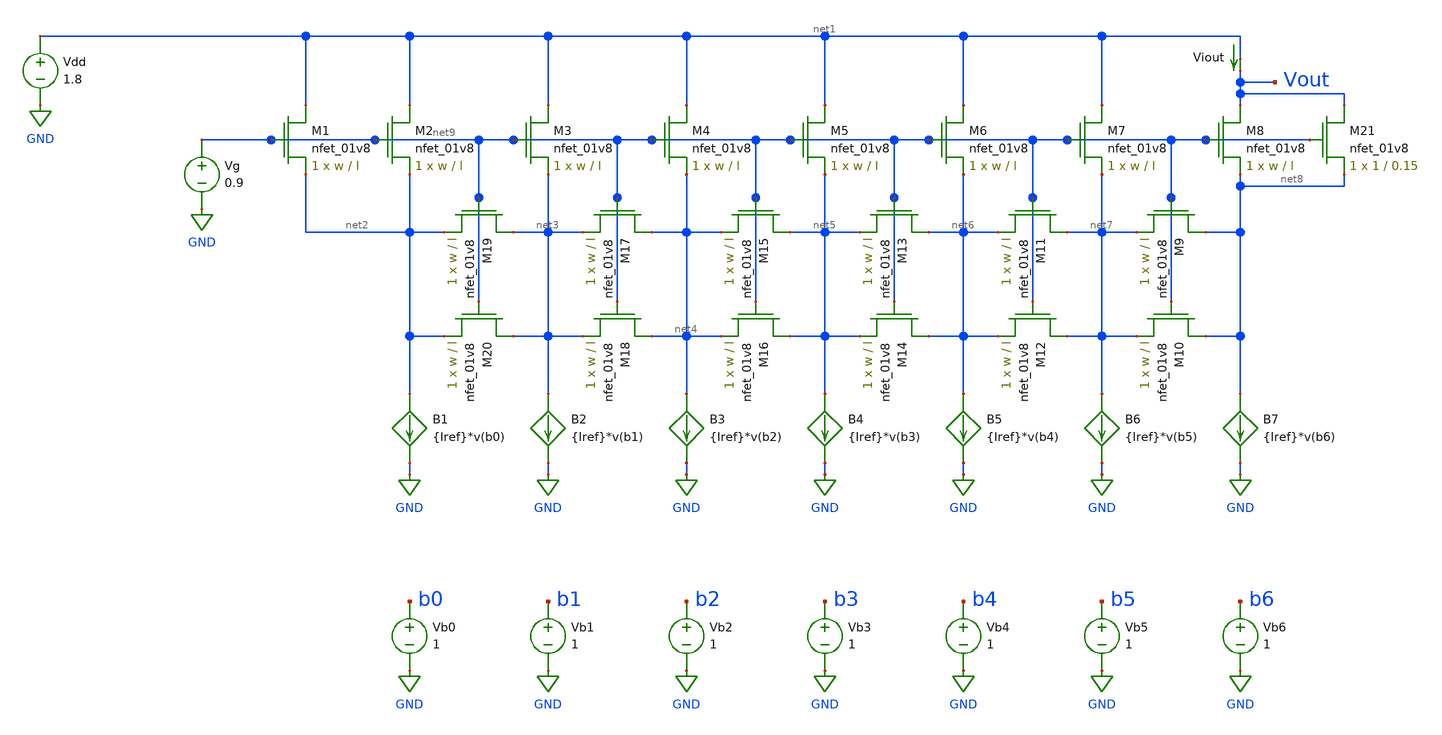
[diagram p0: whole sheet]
** sch_path: simulations/dactut/dactut/dactut_mosfet.sch
**.subckt dactut_mosfet
B1 net2 GND I={Iref}*v(b0)
Vb0 b0 GND 1
Viout net1 Vout 0
.save i(viout)
B2 net3 GND I={Iref}*v(b1)
Vb1 b1 GND 1
B3 net4 GND I={Iref}*v(b2)
Vb2 b2 GND 1
B4 net5 GND I={Iref}*v(b3)
Vb3 b3 GND 1
B5 net6 GND I={Iref}*v(b4)
Vb4 b4 GND 1
B6 net7 GND I={Iref}*v(b5)
Vb5 b5 GND 1
B7 net8 GND I={Iref}*v(b6)
Vb6 b6 GND 1
Vdd net1 GND 1.8
Vg net9 GND 0.9
XM1 net1 net9 net2 GND sky130_fd_pr__nfet_01v8 L=l W=w nf=1 ad='int((nf+1)/2) * W/nf * 0.29' as='int((nf+2)/2) * W/nf * 0.29'
+ pd='2*int((nf+1)/2) * (W/nf + 0.29)' ps='2*int((nf+2)/2) * (W/nf + 0.29)' nrd='0.29 / W' nrs='0.29 / W'
+ sa=0 sb=0 sd=0 mult=1 m=1
XM21 Vout net9 net8 GND sky130_fd_pr__nfet_01v8 L=0.15 W=1 nf=1 ad='int((nf+1)/2) * W/nf * 0.29' as='int((nf+2)/2) * W/nf * 0.29'
+ pd='2*int((nf+1)/2) * (W/nf + 0.29)' ps='2*int((nf+2)/2) * (W/nf + 0.29)' nrd='0.29 / W' nrs='0.29 / W'
+ sa=0 sb=0 sd=0 mult=1 m=1
XM2 net1 net9 net2 GND sky130_fd_pr__nfet_01v8 L=l W=w nf=1 ad='int((nf+1)/2) * W/nf * 0.29' as='int((nf+2)/2) * W/nf * 0.29'
+ pd='2*int((nf+1)/2) * (W/nf + 0.29)' ps='2*int((nf+2)/2) * (W/nf + 0.29)' nrd='0.29 / W' nrs='0.29 / W'
+ sa=0 sb=0 sd=0 mult=1 m=1
XM3 net1 net9 net3 GND sky130_fd_pr__nfet_01v8 L=l W=w nf=1 ad='int((nf+1)/2) * W/nf * 0.29' as='int((nf+2)/2) * W/nf * 0.29'
+ pd='2*int((nf+1)/2) * (W/nf + 0.29)' ps='2*int((nf+2)/2) * (W/nf + 0.29)' nrd='0.29 / W' nrs='0.29 / W'
+ sa=0 sb=0 sd=0 mult=1 m=1
XM4 net1 net9 net4 GND sky130_fd_pr__nfet_01v8 L=l W=w nf=1 ad='int((nf+1)/2) * W/nf * 0.29' as='int((nf+2)/2) * W/nf * 0.29'
+ pd='2*int((nf+1)/2) * (W/nf + 0.29)' ps='2*int((nf+2)/2) * (W/nf + 0.29)' nrd='0.29 / W' nrs='0.29 / W'
+ sa=0 sb=0 sd=0 mult=1 m=1
XM5 net1 net9 net5 GND sky130_fd_pr__nfet_01v8 L=l W=w nf=1 ad='int((nf+1)/2) * W/nf * 0.29' as='int((nf+2)/2) * W/nf * 0.29'
+ pd='2*int((nf+1)/2) * (W/nf + 0.29)' ps='2*int((nf+2)/2) * (W/nf + 0.29)' nrd='0.29 / W' nrs='0.29 / W'
+ sa=0 sb=0 sd=0 mult=1 m=1
XM6 net1 net9 net6 GND sky130_fd_pr__nfet_01v8 L=l W=w nf=1 ad='int((nf+1)/2) * W/nf * 0.29' as='int((nf+2)/2) * W/nf * 0.29'
+ pd='2*int((nf+1)/2) * (W/nf + 0.29)' ps='2*int((nf+2)/2) * (W/nf + 0.29)' nrd='0.29 / W' nrs='0.29 / W'
+ sa=0 sb=0 sd=0 mult=1 m=1
XM7 net1 net9 net7 GND sky130_fd_pr__nfet_01v8 L=l W=w nf=1 ad='int((nf+1)/2) * W/nf * 0.29' as='int((nf+2)/2) * W/nf * 0.29'
+ pd='2*int((nf+1)/2) * (W/nf + 0.29)' ps='2*int((nf+2)/2) * (W/nf + 0.29)' nrd='0.29 / W' nrs='0.29 / W'
+ sa=0 sb=0 sd=0 mult=1 m=1
XM8 Vout net9 net8 GND sky130_fd_pr__nfet_01v8 L=l W=w nf=1 ad='int((nf+1)/2) * W/nf * 0.29' as='int((nf+2)/2) * W/nf * 0.29'
+ pd='2*int((nf+1)/2) * (W/nf + 0.29)' ps='2*int((nf+2)/2) * (W/nf + 0.29)' nrd='0.29 / W' nrs='0.29 / W'
+ sa=0 sb=0 sd=0 mult=1 m=1
XM9 net8 net9 net7 GND sky130_fd_pr__nfet_01v8 L=l W=w nf=1 ad='int((nf+1)/2) * W/nf * 0.29' as='int((nf+2)/2) * W/nf * 0.29'
+ pd='2*int((nf+1)/2) * (W/nf + 0.29)' ps='2*int((nf+2)/2) * (W/nf + 0.29)' nrd='0.29 / W' nrs='0.29 / W'
+ sa=0 sb=0 sd=0 mult=1 m=1
XM10 net8 net9 net7 GND sky130_fd_pr__nfet_01v8 L=l W=w nf=1 ad='int((nf+1)/2) * W/nf * 0.29' as='int((nf+2)/2) * W/nf * 0.29'
+ pd='2*int((nf+1)/2) * (W/nf + 0.29)' ps='2*int((nf+2)/2) * (W/nf + 0.29)' nrd='0.29 / W' nrs='0.29 / W'
+ sa=0 sb=0 sd=0 mult=1 m=1
XM11 net7 net9 net6 GND sky130_fd_pr__nfet_01v8 L=l W=w nf=1 ad='int((nf+1)/2) * W/nf * 0.29' as='int((nf+2)/2) * W/nf * 0.29'
+ pd='2*int((nf+1)/2) * (W/nf + 0.29)' ps='2*int((nf+2)/2) * (W/nf + 0.29)' nrd='0.29 / W' nrs='0.29 / W'
+ sa=0 sb=0 sd=0 mult=1 m=1
XM12 net7 net9 net6 GND sky130_fd_pr__nfet_01v8 L=l W=w nf=1 ad='int((nf+1)/2) * W/nf * 0.29' as='int((nf+2)/2) * W/nf * 0.29'
+ pd='2*int((nf+1)/2) * (W/nf + 0.29)' ps='2*int((nf+2)/2) * (W/nf + 0.29)' nrd='0.29 / W' nrs='0.29 / W'
+ sa=0 sb=0 sd=0 mult=1 m=1
XM13 net6 net9 net5 GND sky130_fd_pr__nfet_01v8 L=l W=w nf=1 ad='int((nf+1)/2) * W/nf * 0.29' as='int((nf+2)/2) * W/nf * 0.29'
+ pd='2*int((nf+1)/2) * (W/nf + 0.29)' ps='2*int((nf+2)/2) * (W/nf + 0.29)' nrd='0.29 / W' nrs='0.29 / W'
+ sa=0 sb=0 sd=0 mult=1 m=1
XM14 net6 net9 net5 GND sky130_fd_pr__nfet_01v8 L=l W=w nf=1 ad='int((nf+1)/2) * W/nf * 0.29' as='int((nf+2)/2) * W/nf * 0.29'
+ pd='2*int((nf+1)/2) * (W/nf + 0.29)' ps='2*int((nf+2)/2) * (W/nf + 0.29)' nrd='0.29 / W' nrs='0.29 / W'
+ sa=0 sb=0 sd=0 mult=1 m=1
XM15 net5 net9 net4 GND sky130_fd_pr__nfet_01v8 L=l W=w nf=1 ad='int((nf+1)/2) * W/nf * 0.29' as='int((nf+2)/2) * W/nf * 0.29'
+ pd='2*int((nf+1)/2) * (W/nf + 0.29)' ps='2*int((nf+2)/2) * (W/nf + 0.29)' nrd='0.29 / W' nrs='0.29 / W'
+ sa=0 sb=0 sd=0 mult=1 m=1
XM16 net5 net9 net4 GND sky130_fd_pr__nfet_01v8 L=l W=w nf=1 ad='int((nf+1)/2) * W/nf * 0.29' as='int((nf+2)/2) * W/nf * 0.29'
+ pd='2*int((nf+1)/2) * (W/nf + 0.29)' ps='2*int((nf+2)/2) * (W/nf + 0.29)' nrd='0.29 / W' nrs='0.29 / W'
+ sa=0 sb=0 sd=0 mult=1 m=1
XM17 net4 net9 net3 GND sky130_fd_pr__nfet_01v8 L=l W=w nf=1 ad='int((nf+1)/2) * W/nf * 0.29' as='int((nf+2)/2) * W/nf * 0.29'
+ pd='2*int((nf+1)/2) * (W/nf + 0.29)' ps='2*int((nf+2)/2) * (W/nf + 0.29)' nrd='0.29 / W' nrs='0.29 / W'
+ sa=0 sb=0 sd=0 mult=1 m=1
XM18 net4 net9 net3 GND sky130_fd_pr__nfet_01v8 L=l W=w nf=1 ad='int((nf+1)/2) * W/nf * 0.29' as='int((nf+2)/2) * W/nf * 0.29'
+ pd='2*int((nf+1)/2) * (W/nf + 0.29)' ps='2*int((nf+2)/2) * (W/nf + 0.29)' nrd='0.29 / W' nrs='0.29 / W'
+ sa=0 sb=0 sd=0 mult=1 m=1
XM19 net3 net9 net2 GND sky130_fd_pr__nfet_01v8 L=l W=w nf=1 ad='int((nf+1)/2) * W/nf * 0.29' as='int((nf+2)/2) * W/nf * 0.29'
+ pd='2*int((nf+1)/2) * (W/nf + 0.29)' ps='2*int((nf+2)/2) * (W/nf + 0.29)' nrd='0.29 / W' nrs='0.29 / W'
+ sa=0 sb=0 sd=0 mult=1 m=1
XM20 net3 net9 net2 GND sky130_fd_pr__nfet_01v8 L=l W=w nf=1 ad='int((nf+1)/2) * W/nf * 0.29' as='int((nf+2)/2) * W/nf * 0.29'
+ pd='2*int((nf+1)/2) * (W/nf + 0.29)' ps='2*int((nf+2)/2) * (W/nf + 0.29)' nrd='0.29 / W' nrs='0.29 / W'
+ sa=0 sb=0 sd=0 mult=1 m=1
**** begin user architecture code

.param Iref=100u
.param MC_SWITCH = 0.0
.param l=8
.param w=4
.control
  set wr_vecnames
  set wr_singlescale
  let code = 0
  while code < 128
    if code eq 0
      let b0 = 0
    else
      let b0 = code % 2
    end
    if floor(code / 2) eq 0
      let b1 = 0
    else
      let b1 = floor(code / 2) % 2
    end
    if floor(code / 4) eq 0
      let b2 = 0
    else
      let b2 = floor(code / 4) % 2
    end
    if floor(code / 8) eq 0
      let b3 = 0
    else
      let b3 = floor(code / 8) % 2
    end
    if floor(code / 16) eq 0
      let b4 = 0
    else
      let b4 = floor(code / 16) % 2
    end
    if floor(code / 32) eq 0
      let b5 = 0
    else
      let b5 = floor(code / 32) % 2
    end
    if floor(code / 64) eq 0
      let b6 = 0
    else
      let b6 = floor(code / 64) % 2
    end
    alter vb0 $&b0
    alter vb1 $&b1
    alter vb2 $&b2
    alter vb3 $&b3
    alter vb4 $&b4
    alter vb5 $&b5
    alter vb6 $&b6
    save all
    op
    wrdata ~/Documents/dactut/dactut.txt v(b0) v(b1) v(b2) v(b3) v(b4) v(b5) v(b6) i(Viout) v(Vout)
    if code eq 0
      set appendwrite
      set wr_vecnames = FALSE
    end
    let code = code + 1
  end
  quit
.endc
.lib ~/skywater/skywater-pdk/libraries/sky130_fd_pr_ngspice/latest/models/sky130.lib.spice tt

**** end user architecture code
**.ends
.GLOBAL GND
.end
